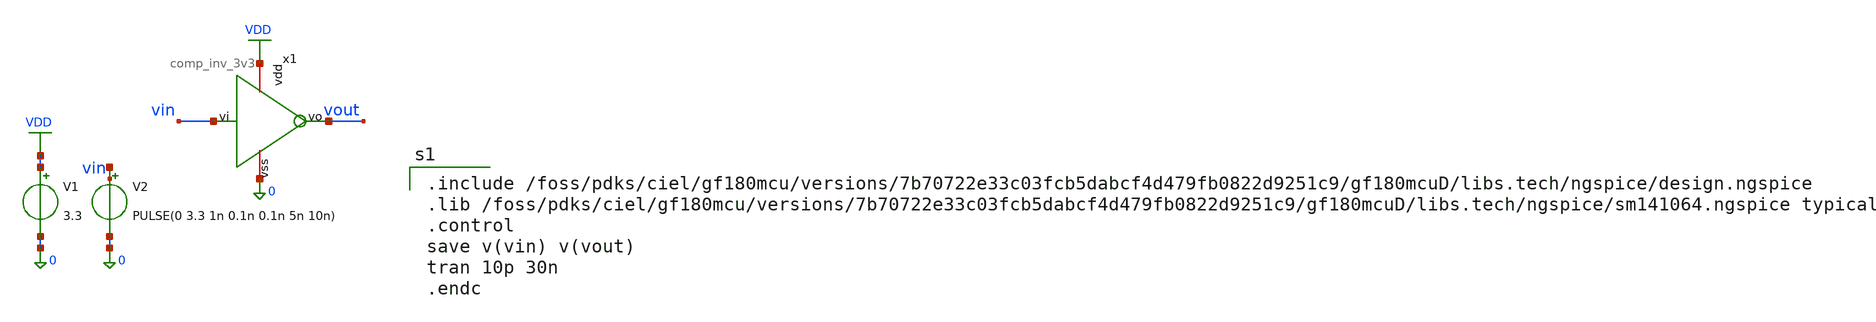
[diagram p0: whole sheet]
** sch_path: xschem/sar_adc/blocks/comparator/testbench/tb_comp_inv_3v3.sch
**.subckt tb_comp_inv_3v3
x1 VDD vin vout 0 comp_inv_3v3
V1 VDD 0 3.3
V2 vin 0 PULSE(0 3.3 1n 0.1n 0.1n 5n 10n)
**** begin user architecture code

.include /foss/pdks/ciel/gf180mcu/versions/7b70722e33c03fcb5dabcf4d479fb0822d9251c9/gf180mcuD/libs.tech/ngspice/design.ngspice
.lib /foss/pdks/ciel/gf180mcu/versions/7b70722e33c03fcb5dabcf4d479fb0822d9251c9/gf180mcuD/libs.tech/ngspice/sm141064.ngspice typical
.control
save v(vin) v(vout)
tran 10p 30n
.endc

**** end user architecture code
**.ends

* expanding   symbol:  sar_adc/blocks/comparator/comp_inv_3v3.sym # of pins=4
** sym_path: xschem/sar_adc/blocks/comparator/comp_inv_3v3.sym
** sch_path: xschem/sar_adc/blocks/comparator/comp_inv_3v3.sch
.subckt comp_inv_3v3 vdd vi vo vss
*.ipin vi
*.opin vo
*.iopin vdd
*.iopin vss
XM2 vo vi vdd vdd pfet_03v3 L=0.28u W=3.20u nf=1 ad='int((nf+1)/2) * W/nf * 0.18u' as='int((nf+2)/2) * W/nf * 0.18u'
+ pd='2*int((nf+1)/2) * (W/nf + 0.18u)' ps='2*int((nf+2)/2) * (W/nf + 0.18u)' nrd='0.18u / W' nrs='0.18u / W'
+ sa=0 sb=0 sd=0 m=1
XM1 vo vi vss vss nfet_03v3 L=0.28u W=1.60u nf=1 ad='int((nf+1)/2) * W/nf * 0.18u' as='int((nf+2)/2) * W/nf * 0.18u'
+ pd='2*int((nf+1)/2) * (W/nf + 0.18u)' ps='2*int((nf+2)/2) * (W/nf + 0.18u)' nrd='0.18u / W' nrs='0.18u / W'
+ sa=0 sb=0 sd=0 m=1
.ends

.GLOBAL VDD
.end
